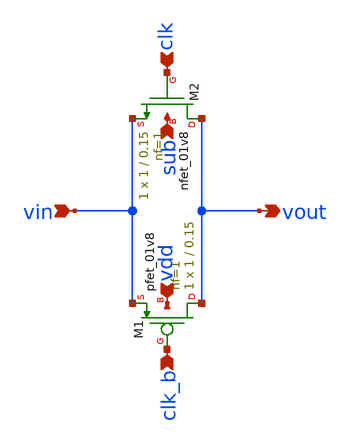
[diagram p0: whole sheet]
** sch_path: top/test/design/tg_final.sch
**.subckt tg_final clk vin vout vdd sub clk_b
*.ipin clk
*.ipin vin
*.opin vout
*.ipin vdd
*.ipin sub
*.ipin clk_b
XM2 vout clk vin sub sky130_fd_pr__nfet_01v8 L=0.15 W=1 nf=1 ad='int((nf+1)/2) * W/nf * 0.29' as='int((nf+2)/2) * W/nf * 0.29'
+ pd='2*int((nf+1)/2) * (W/nf + 0.29)' ps='2*int((nf+2)/2) * (W/nf + 0.29)' nrd='0.29 / W' nrs='0.29 / W'
+ sa=0 sb=0 sd=0 mult=1 m=1
XM1 vout clk_b vin vdd sky130_fd_pr__pfet_01v8 L=0.15 W=1 nf=1 ad='int((nf+1)/2) * W/nf * 0.29' as='int((nf+2)/2) * W/nf * 0.29'
+ pd='2*int((nf+1)/2) * (W/nf + 0.29)' ps='2*int((nf+2)/2) * (W/nf + 0.29)' nrd='0.29 / W' nrs='0.29 / W'
+ sa=0 sb=0 sd=0 mult=1 m=1
**.ends
.end
